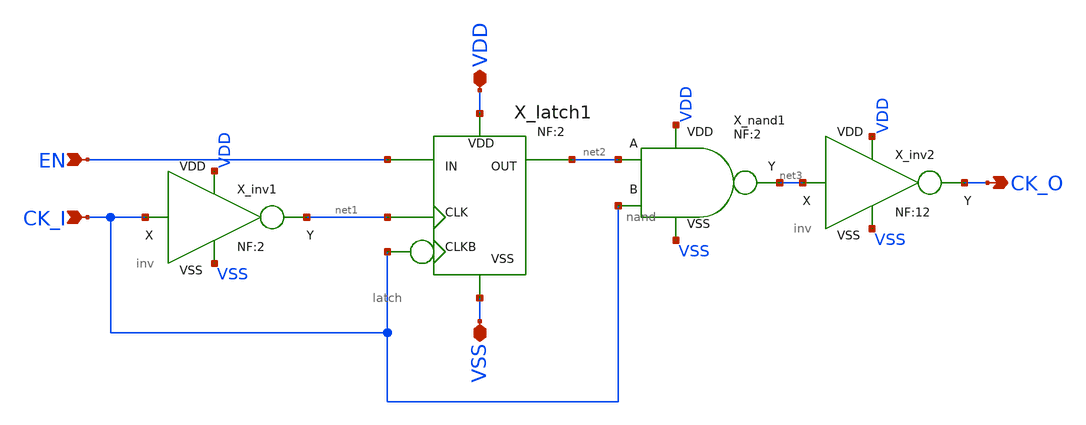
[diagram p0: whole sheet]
** sch_path: xschem_lib/DFFRAM_full_custom/clk_gate.sch
**.subckt clk_gate CK_I VDD VSS EN CK_O
*.ipin CK_I
*.iopin VDD
*.iopin VSS
*.ipin EN
*.opin CK_O
X_inv1 CK_I VDD VSS net1 inv NF=2
X_latch1 EN net1 CK_I VSS VDD net2 latch NF=2
X_nand1 CK_I net2 net3 VDD VSS nand NF=2
X_inv2 net3 VDD VSS CK_O inv NF=12
**.ends
.end
